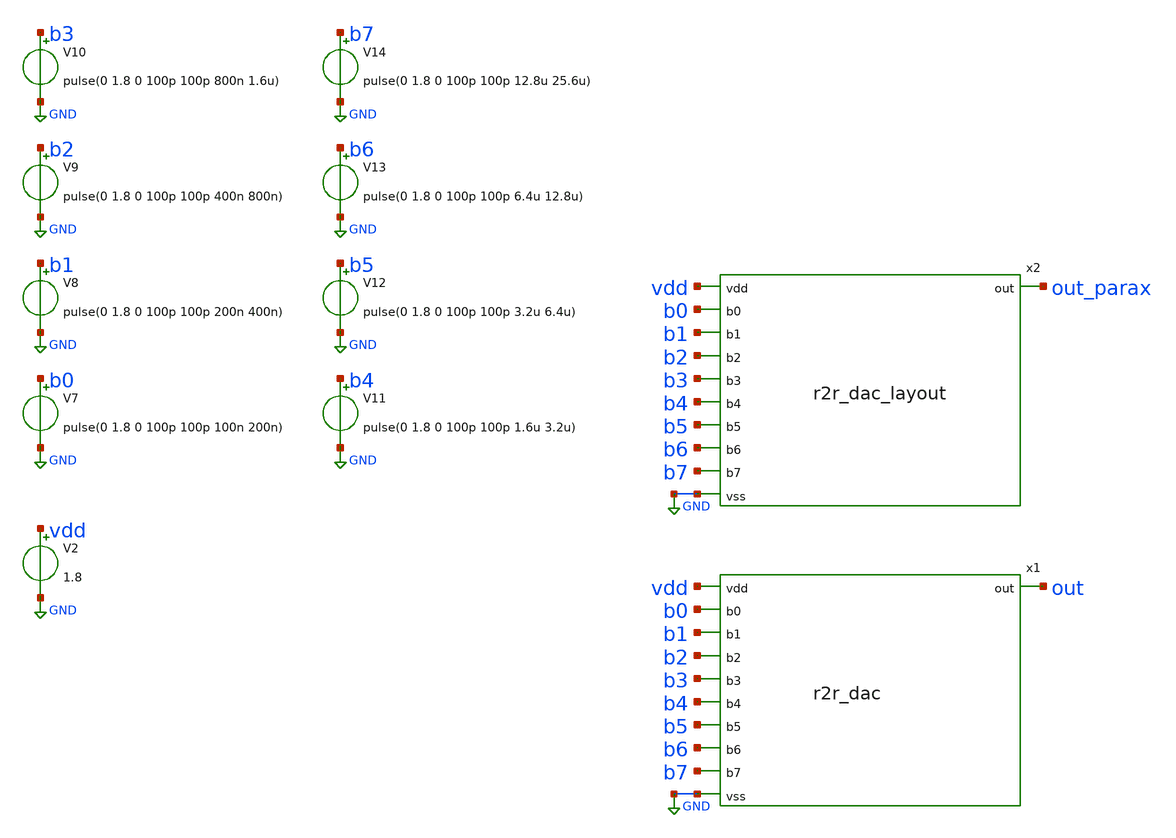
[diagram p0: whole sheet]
** sch_path: custom_gds/tt_um_tim2305_adc_dac/xschem/r2r_dac_tb.sch
**.subckt r2r_dac_tb
V2 vdd GND 1.8
V7 b0 GND pulse(0 1.8 0 100p 100p 100n 200n)
V8 b1 GND pulse(0 1.8 0 100p 100p 200n 400n)
V9 b2 GND pulse(0 1.8 0 100p 100p 400n 800n)
V10 b3 GND pulse(0 1.8 0 100p 100p 800n 1.6u)
V11 b4 GND pulse(0 1.8 0 100p 100p 1.6u 3.2u)
V12 b5 GND pulse(0 1.8 0 100p 100p 3.2u 6.4u)
V13 b6 GND pulse(0 1.8 0 100p 100p 6.4u 12.8u)
V14 b7 GND pulse(0 1.8 0 100p 100p 12.8u 25.6u)
x1 out vdd b0 b1 b2 b3 b4 b5 b6 b7 GND r2r_dac
x2 out_parax vdd b0 b1 b2 b3 b4 b5 b6 b7 GND r2r_dac_layout
**** begin user architecture code


.tran 10n 25.6u
.save all
.lib /home/ttuser/pdk/sky130A/libs.tech/ngspice/sky130.lib.spice tt


**** end user architecture code
**.ends

* expanding   symbol:  /home/ttuser/Documents/aprx_adc/r2r_dac.sym # of pins=11
** sym_path: custom_gds/tt_um_tim2305_adc_dac/xschem/r2r_dac.sym
** sch_path: custom_gds/tt_um_tim2305_adc_dac/xschem/r2r_dac.sch
.subckt r2r_dac out vdd b0 b1 b2 b3 b4 b5 b6 b7 vss
*.ipin vdd
*.opin out
*.ipin b0
*.ipin b1
*.ipin b2
*.ipin b3
*.ipin b4
*.ipin b5
*.ipin b6
*.ipin b7
*.ipin vss
XR3 net1 vss net8 sky130_fd_pr__res_xhigh_po_0p35 L=0.35*4 mult=1 m=1
XR1 net1 t0 net9 sky130_fd_pr__res_xhigh_po_0p35 L=0.35*4 mult=1 m=1
XR2 net2 net1 net10 sky130_fd_pr__res_xhigh_po_0p35 L=0.35*2 mult=1 m=1
XR5 net2 t1 net11 sky130_fd_pr__res_xhigh_po_0p35 L=0.35*4 mult=1 m=1
XR6 net3 net2 net12 sky130_fd_pr__res_xhigh_po_0p35 L=0.35*2 mult=1 m=1
XR7 net3 t2 net13 sky130_fd_pr__res_xhigh_po_0p35 L=0.35*4 mult=1 m=1
XR8 net4 net3 net14 sky130_fd_pr__res_xhigh_po_0p35 L=0.35*2 mult=1 m=1
XR9 net4 t3 net15 sky130_fd_pr__res_xhigh_po_0p35 L=0.35*4 mult=1 m=1
XR10 net5 net4 net16 sky130_fd_pr__res_xhigh_po_0p35 L=0.35*2 mult=1 m=1
XR11 net5 t4 net17 sky130_fd_pr__res_xhigh_po_0p35 L=0.35*4 mult=1 m=1
XR12 net6 net5 net18 sky130_fd_pr__res_xhigh_po_0p35 L=0.35*2 mult=1 m=1
XR13 net6 t5 net19 sky130_fd_pr__res_xhigh_po_0p35 L=0.35*4 mult=1 m=1
XR14 net7 net6 net20 sky130_fd_pr__res_xhigh_po_0p35 L=0.35*2 mult=1 m=1
XR15 net7 t6 net21 sky130_fd_pr__res_xhigh_po_0p35 L=0.35*4 mult=1 m=1
XR16 out net7 net22 sky130_fd_pr__res_xhigh_po_0p35 L=0.35*2 mult=1 m=1
XR17 out t7 net23 sky130_fd_pr__res_xhigh_po_0p35 L=0.35*4 mult=1 m=1
XM2 t0 b0 vdd vdd sky130_fd_pr__pfet_01v8 L=0.15 W=6 nf=1 ad='int((nf+1)/2) * W/nf * 0.29' as='int((nf+2)/2) * W/nf * 0.29'
+ pd='2*int((nf+1)/2) * (W/nf + 0.29)' ps='2*int((nf+2)/2) * (W/nf + 0.29)' nrd='0.29 / W' nrs='0.29 / W'
+ sa=0 sb=0 sd=0 mult=1 m=1
XM4 t1 b1 vdd vdd sky130_fd_pr__pfet_01v8 L=0.15 W=6 nf=1 ad='int((nf+1)/2) * W/nf * 0.29' as='int((nf+2)/2) * W/nf * 0.29'
+ pd='2*int((nf+1)/2) * (W/nf + 0.29)' ps='2*int((nf+2)/2) * (W/nf + 0.29)' nrd='0.29 / W' nrs='0.29 / W'
+ sa=0 sb=0 sd=0 mult=1 m=1
XM6 t2 b2 vdd vdd sky130_fd_pr__pfet_01v8 L=0.15 W=6 nf=1 ad='int((nf+1)/2) * W/nf * 0.29' as='int((nf+2)/2) * W/nf * 0.29'
+ pd='2*int((nf+1)/2) * (W/nf + 0.29)' ps='2*int((nf+2)/2) * (W/nf + 0.29)' nrd='0.29 / W' nrs='0.29 / W'
+ sa=0 sb=0 sd=0 mult=1 m=1
XM8 t3 b3 vdd vdd sky130_fd_pr__pfet_01v8 L=0.15 W=6 nf=1 ad='int((nf+1)/2) * W/nf * 0.29' as='int((nf+2)/2) * W/nf * 0.29'
+ pd='2*int((nf+1)/2) * (W/nf + 0.29)' ps='2*int((nf+2)/2) * (W/nf + 0.29)' nrd='0.29 / W' nrs='0.29 / W'
+ sa=0 sb=0 sd=0 mult=1 m=1
XM10 t4 b4 vdd vdd sky130_fd_pr__pfet_01v8 L=0.15 W=6 nf=1 ad='int((nf+1)/2) * W/nf * 0.29' as='int((nf+2)/2) * W/nf * 0.29'
+ pd='2*int((nf+1)/2) * (W/nf + 0.29)' ps='2*int((nf+2)/2) * (W/nf + 0.29)' nrd='0.29 / W' nrs='0.29 / W'
+ sa=0 sb=0 sd=0 mult=1 m=1
XM12 t5 b5 vdd vdd sky130_fd_pr__pfet_01v8 L=0.15 W=6 nf=1 ad='int((nf+1)/2) * W/nf * 0.29' as='int((nf+2)/2) * W/nf * 0.29'
+ pd='2*int((nf+1)/2) * (W/nf + 0.29)' ps='2*int((nf+2)/2) * (W/nf + 0.29)' nrd='0.29 / W' nrs='0.29 / W'
+ sa=0 sb=0 sd=0 mult=1 m=1
XM14 t6 b6 vdd vdd sky130_fd_pr__pfet_01v8 L=0.15 W=6 nf=1 ad='int((nf+1)/2) * W/nf * 0.29' as='int((nf+2)/2) * W/nf * 0.29'
+ pd='2*int((nf+1)/2) * (W/nf + 0.29)' ps='2*int((nf+2)/2) * (W/nf + 0.29)' nrd='0.29 / W' nrs='0.29 / W'
+ sa=0 sb=0 sd=0 mult=1 m=1
XM16 t7 b7 vdd vdd sky130_fd_pr__pfet_01v8 L=0.15 W=6 nf=1 ad='int((nf+1)/2) * W/nf * 0.29' as='int((nf+2)/2) * W/nf * 0.29'
+ pd='2*int((nf+1)/2) * (W/nf + 0.29)' ps='2*int((nf+2)/2) * (W/nf + 0.29)' nrd='0.29 / W' nrs='0.29 / W'
+ sa=0 sb=0 sd=0 mult=1 m=1
XM1 t0 b0 vss vss sky130_fd_pr__nfet_01v8 L=0.15 W=2 nf=1 ad='int((nf+1)/2) * W/nf * 0.29' as='int((nf+2)/2) * W/nf * 0.29'
+ pd='2*int((nf+1)/2) * (W/nf + 0.29)' ps='2*int((nf+2)/2) * (W/nf + 0.29)' nrd='0.29 / W' nrs='0.29 / W'
+ sa=0 sb=0 sd=0 mult=1 m=1
XM3 t1 b1 vss vss sky130_fd_pr__nfet_01v8 L=0.15 W=2 nf=1 ad='int((nf+1)/2) * W/nf * 0.29' as='int((nf+2)/2) * W/nf * 0.29'
+ pd='2*int((nf+1)/2) * (W/nf + 0.29)' ps='2*int((nf+2)/2) * (W/nf + 0.29)' nrd='0.29 / W' nrs='0.29 / W'
+ sa=0 sb=0 sd=0 mult=1 m=1
XM5 t2 b2 vss vss sky130_fd_pr__nfet_01v8 L=0.15 W=2 nf=1 ad='int((nf+1)/2) * W/nf * 0.29' as='int((nf+2)/2) * W/nf * 0.29'
+ pd='2*int((nf+1)/2) * (W/nf + 0.29)' ps='2*int((nf+2)/2) * (W/nf + 0.29)' nrd='0.29 / W' nrs='0.29 / W'
+ sa=0 sb=0 sd=0 mult=1 m=1
XM7 t3 b3 vss vss sky130_fd_pr__nfet_01v8 L=0.15 W=2 nf=1 ad='int((nf+1)/2) * W/nf * 0.29' as='int((nf+2)/2) * W/nf * 0.29'
+ pd='2*int((nf+1)/2) * (W/nf + 0.29)' ps='2*int((nf+2)/2) * (W/nf + 0.29)' nrd='0.29 / W' nrs='0.29 / W'
+ sa=0 sb=0 sd=0 mult=1 m=1
XM9 t4 b4 vss vss sky130_fd_pr__nfet_01v8 L=0.15 W=2 nf=1 ad='int((nf+1)/2) * W/nf * 0.29' as='int((nf+2)/2) * W/nf * 0.29'
+ pd='2*int((nf+1)/2) * (W/nf + 0.29)' ps='2*int((nf+2)/2) * (W/nf + 0.29)' nrd='0.29 / W' nrs='0.29 / W'
+ sa=0 sb=0 sd=0 mult=1 m=1
XM11 t5 b5 vss vss sky130_fd_pr__nfet_01v8 L=0.15 W=2 nf=1 ad='int((nf+1)/2) * W/nf * 0.29' as='int((nf+2)/2) * W/nf * 0.29'
+ pd='2*int((nf+1)/2) * (W/nf + 0.29)' ps='2*int((nf+2)/2) * (W/nf + 0.29)' nrd='0.29 / W' nrs='0.29 / W'
+ sa=0 sb=0 sd=0 mult=1 m=1
XM13 t6 b6 vss vss sky130_fd_pr__nfet_01v8 L=0.15 W=2 nf=1 ad='int((nf+1)/2) * W/nf * 0.29' as='int((nf+2)/2) * W/nf * 0.29'
+ pd='2*int((nf+1)/2) * (W/nf + 0.29)' ps='2*int((nf+2)/2) * (W/nf + 0.29)' nrd='0.29 / W' nrs='0.29 / W'
+ sa=0 sb=0 sd=0 mult=1 m=1
XM15 t7 b7 vss vss sky130_fd_pr__nfet_01v8 L=0.15 W=2 nf=1 ad='int((nf+1)/2) * W/nf * 0.29' as='int((nf+2)/2) * W/nf * 0.29'
+ pd='2*int((nf+1)/2) * (W/nf + 0.29)' ps='2*int((nf+2)/2) * (W/nf + 0.29)' nrd='0.29 / W' nrs='0.29 / W'
+ sa=0 sb=0 sd=0 mult=1 m=1
.ends


* expanding   symbol:  /home/ttuser/Documents/aprx_adc/r2r_dac_layout.sym # of pins=11
** sym_path: custom_gds/tt_um_tim2305_adc_dac/xschem/r2r_dac.sym
.include [abs_sym_path r2r_dac_layout.cir]
.GLOBAL GND
.end
